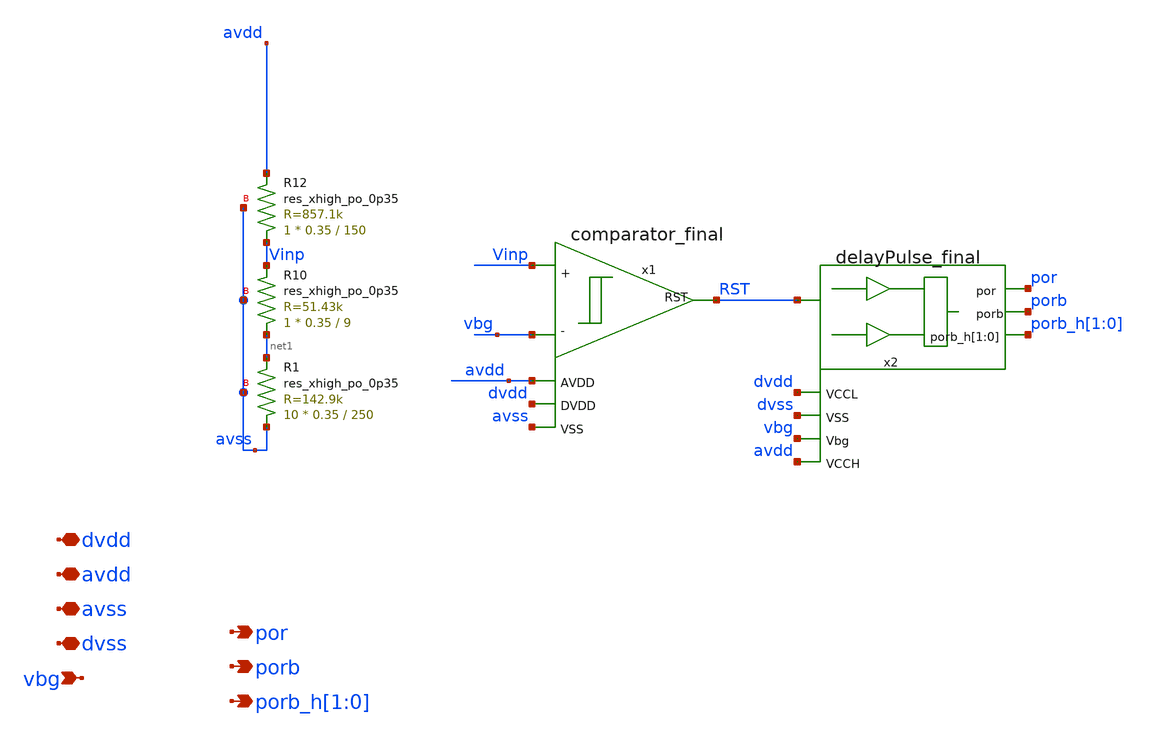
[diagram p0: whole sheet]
** sch_path: xschem/sky130_sw_ip__bgrref_por_dev.sch
**.subckt sky130_sw_ip__bgrref_por_dev avdd por avss dvdd porb vbg porb_h[1],porb_h[0] dvss
*.iopin avdd
*.opin por
*.iopin avss
*.iopin dvdd
*.opin porb
*.ipin vbg
*.opin porb_h[1],porb_h[0]
*.iopin dvss
x1 vbg Vinp RST avss avdd dvdd comparator_final
XR1 avss net1 avss sky130_fd_pr__res_xhigh_po_0p35 L=250 mult=10 m=10
XR10 net1 Vinp avss sky130_fd_pr__res_xhigh_po_0p35 L=9 mult=1 m=1
XR12 Vinp avdd avss sky130_fd_pr__res_xhigh_po_0p35 L=150 mult=1 m=1
x2 RST por dvdd dvss vbg avdd porb porb_h[1] porb_h[0] delayPulse_final
**.ends
.end
